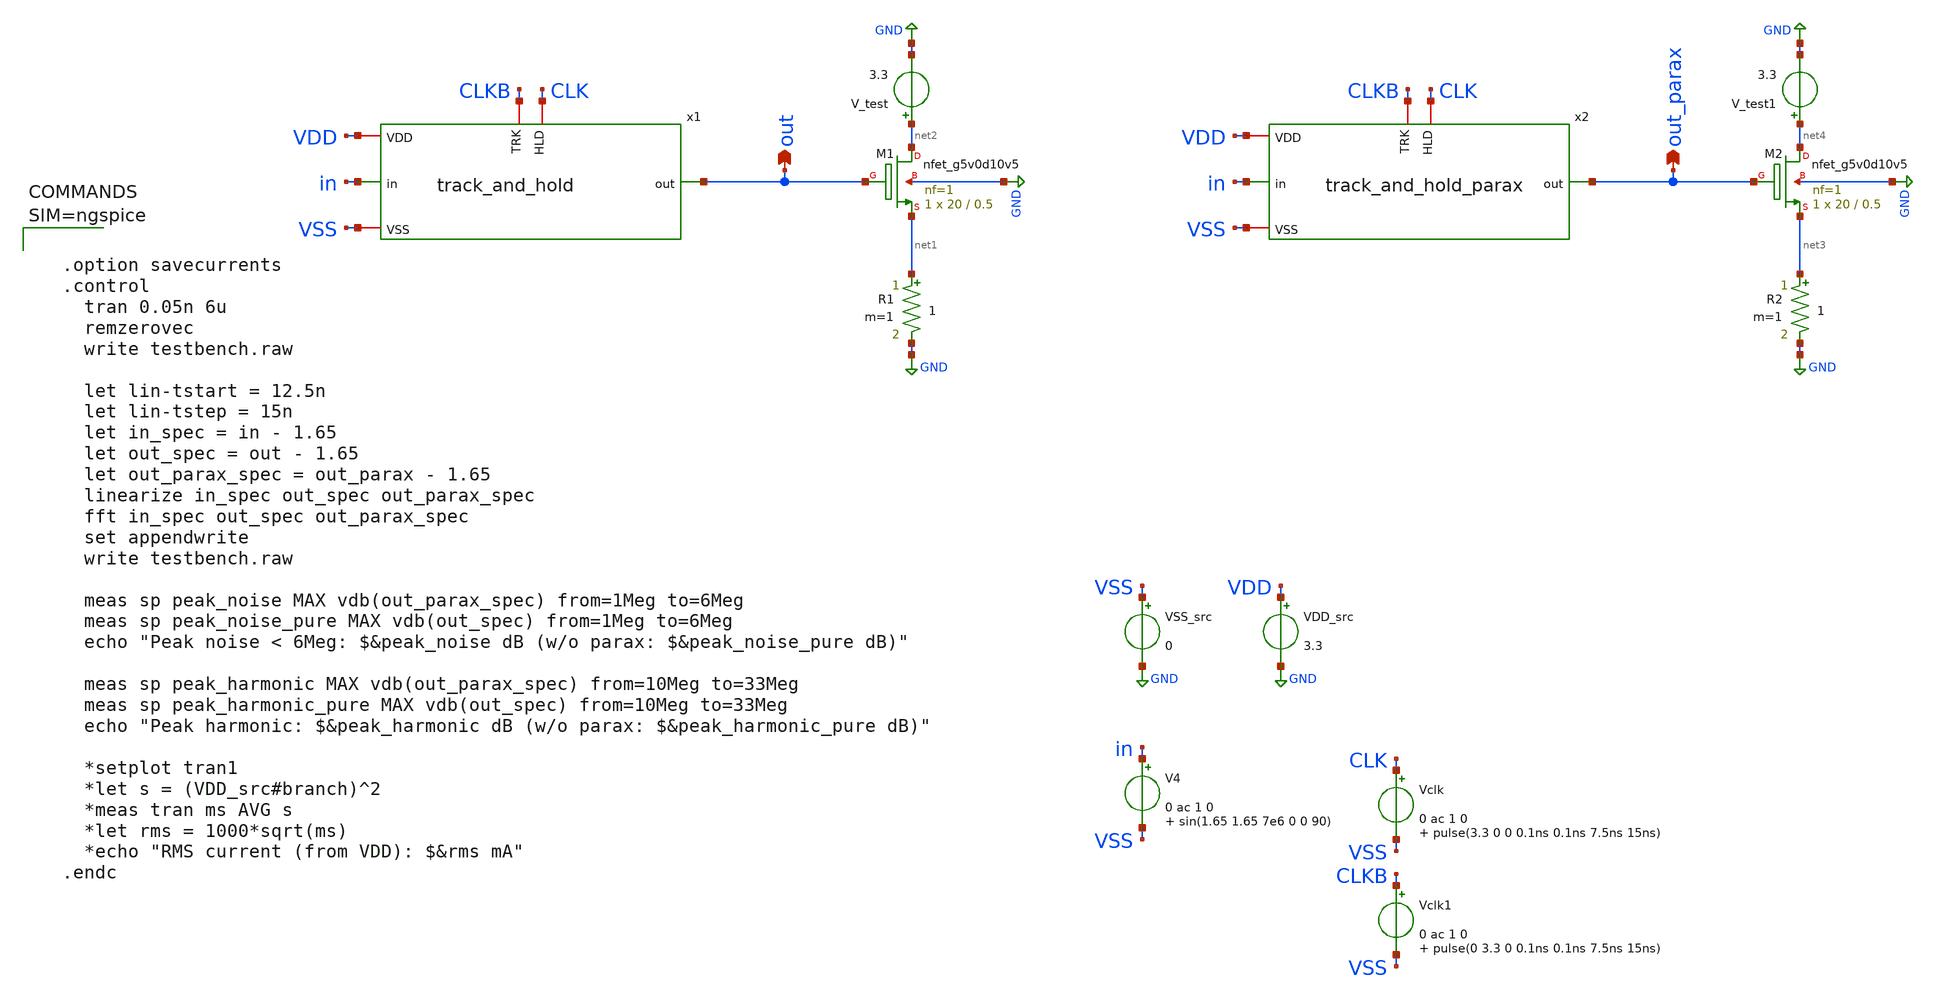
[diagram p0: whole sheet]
** sch_path: xschem/track_and_hold/testbench.sch
**.subckt testbench out out_parax
*.opin out
*.opin out_parax
VDD_src VDD GND 3.3
VSS_src VSS GND 0
V4 in VSS 0 ac 1 0 sin(1.65 1.65 7e6 0 0 90)
XM1 net2 out net1 GND sky130_fd_pr__nfet_g5v0d10v5 L=0.5 W=20 nf=1 ad='int((nf+1)/2) * W/nf * 0.29' as='int((nf+2)/2) * W/nf * 0.29'
+ pd='2*int((nf+1)/2) * (W/nf + 0.29)' ps='2*int((nf+2)/2) * (W/nf + 0.29)' nrd='0.29 / W' nrs='0.29 / W'
+ sa=0 sb=0 sd=0 mult=1 m=1
R1 net1 GND 1 m=1
Vclk CLK VSS 0 ac 1 0 pulse(3.3 0 0 0.1ns 0.1ns 7.5ns 15ns)
Vclk1 CLKB VSS 0 ac 1 0 pulse(0 3.3 0 0.1ns 0.1ns 7.5ns 15ns)
V_test net2 GND 3.3
XM2 net4 out_parax net3 GND sky130_fd_pr__nfet_g5v0d10v5 L=0.5 W=20 nf=1 ad='int((nf+1)/2) * W/nf * 0.29'
+ as='int((nf+2)/2) * W/nf * 0.29' pd='2*int((nf+1)/2) * (W/nf + 0.29)' ps='2*int((nf+2)/2) * (W/nf + 0.29)'
+ nrd='0.29 / W' nrs='0.29 / W' sa=0 sb=0 sd=0 mult=1 m=1
R2 net3 GND 1 m=1
V_test1 net4 GND 3.3
x1 CLK CLKB VDD VSS out in track_and_hold
x2 CLK CLKB VDD VSS out_parax in track_and_hold_parax
**** begin user architecture code

** opencircuitdesign pdks install
.lib $::SKYWATER_MODELS/sky130.lib.spice tt





  .option savecurrents
  .control
    tran 0.05n 6u
    remzerovec
    write testbench.raw

    let lin-tstart = 12.5n
    let lin-tstep = 15n
    let in_spec = in - 1.65
    let out_spec = out - 1.65
    let out_parax_spec = out_parax - 1.65
    linearize in_spec out_spec out_parax_spec
    fft in_spec out_spec out_parax_spec
    set appendwrite
    write testbench.raw

    meas sp peak_noise MAX vdb(out_parax_spec) from=1Meg to=6Meg
    meas sp peak_noise_pure MAX vdb(out_spec) from=1Meg to=6Meg
    echo "Peak noise < 6Meg: $&peak_noise dB (w/o parax: $&peak_noise_pure dB)"

    meas sp peak_harmonic MAX vdb(out_parax_spec) from=10Meg to=33Meg
    meas sp peak_harmonic_pure MAX vdb(out_spec) from=10Meg to=33Meg
    echo "Peak harmonic: $&peak_harmonic dB (w/o parax: $&peak_harmonic_pure dB)"

    *setplot tran1
    *let s = (VDD_src#branch)^2
    *meas tran ms AVG s
    *let rms = 1000*sqrt(ms)
    *echo "RMS current (from VDD): $&rms mA"
  .endc



**** end user architecture code
**.ends
.GLOBAL GND
.end
